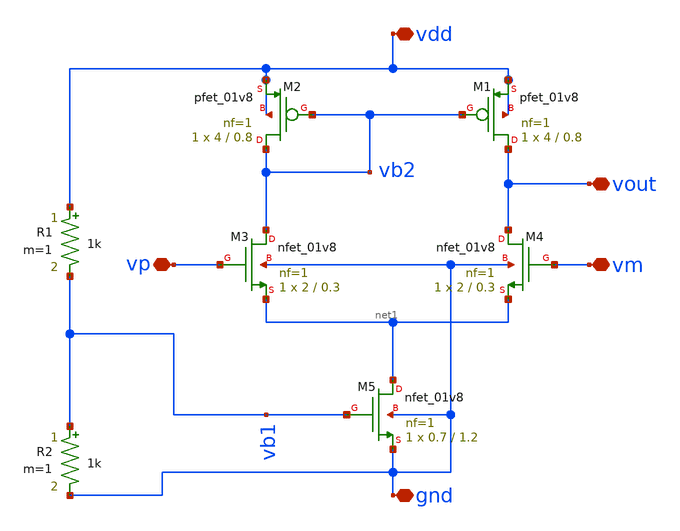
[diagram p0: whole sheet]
** sch_path: OPAMP/opamp_mini.sch
**.subckt opamp_mini vdd gnd vout vm vp
*.iopin vdd
*.iopin gnd
*.iopin vout
*.iopin vm
*.iopin vp
XM1 vout vb2 vdd vdd sky130_fd_pr__pfet_01v8 L=0.8 W=4 nf=1 ad='int((nf+1)/2) * W/nf * 0.29' as='int((nf+2)/2) * W/nf * 0.29'
+ pd='2*int((nf+1)/2) * (W/nf + 0.29)' ps='2*int((nf+2)/2) * (W/nf + 0.29)' nrd='0.29 / W' nrs='0.29 / W'
+ sa=0 sb=0 sd=0 mult=1 m=1
XM2 vb2 vb2 vdd vdd sky130_fd_pr__pfet_01v8 L=0.8 W=4 nf=1 ad='int((nf+1)/2) * W/nf * 0.29' as='int((nf+2)/2) * W/nf * 0.29'
+ pd='2*int((nf+1)/2) * (W/nf + 0.29)' ps='2*int((nf+2)/2) * (W/nf + 0.29)' nrd='0.29 / W' nrs='0.29 / W'
+ sa=0 sb=0 sd=0 mult=1 m=1
XM3 vb2 vp net1 gnd sky130_fd_pr__nfet_01v8 L=0.3 W=2 nf=1 ad='int((nf+1)/2) * W/nf * 0.29' as='int((nf+2)/2) * W/nf * 0.29'
+ pd='2*int((nf+1)/2) * (W/nf + 0.29)' ps='2*int((nf+2)/2) * (W/nf + 0.29)' nrd='0.29 / W' nrs='0.29 / W'
+ sa=0 sb=0 sd=0 mult=1 m=1
XM4 vout vm net1 gnd sky130_fd_pr__nfet_01v8 L=0.3 W=2 nf=1 ad='int((nf+1)/2) * W/nf * 0.29' as='int((nf+2)/2) * W/nf * 0.29'
+ pd='2*int((nf+1)/2) * (W/nf + 0.29)' ps='2*int((nf+2)/2) * (W/nf + 0.29)' nrd='0.29 / W' nrs='0.29 / W'
+ sa=0 sb=0 sd=0 mult=1 m=1
XM5 net1 vb1 gnd gnd sky130_fd_pr__nfet_01v8 L=1.2 W=0.7 nf=1 ad='int((nf+1)/2) * W/nf * 0.29' as='int((nf+2)/2) * W/nf * 0.29'
+ pd='2*int((nf+1)/2) * (W/nf + 0.29)' ps='2*int((nf+2)/2) * (W/nf + 0.29)' nrd='0.29 / W' nrs='0.29 / W'
+ sa=0 sb=0 sd=0 mult=1 m=1
R1 vdd vb1 1k m=1
R2 vb1 gnd 1k m=1
**.ends
.end
